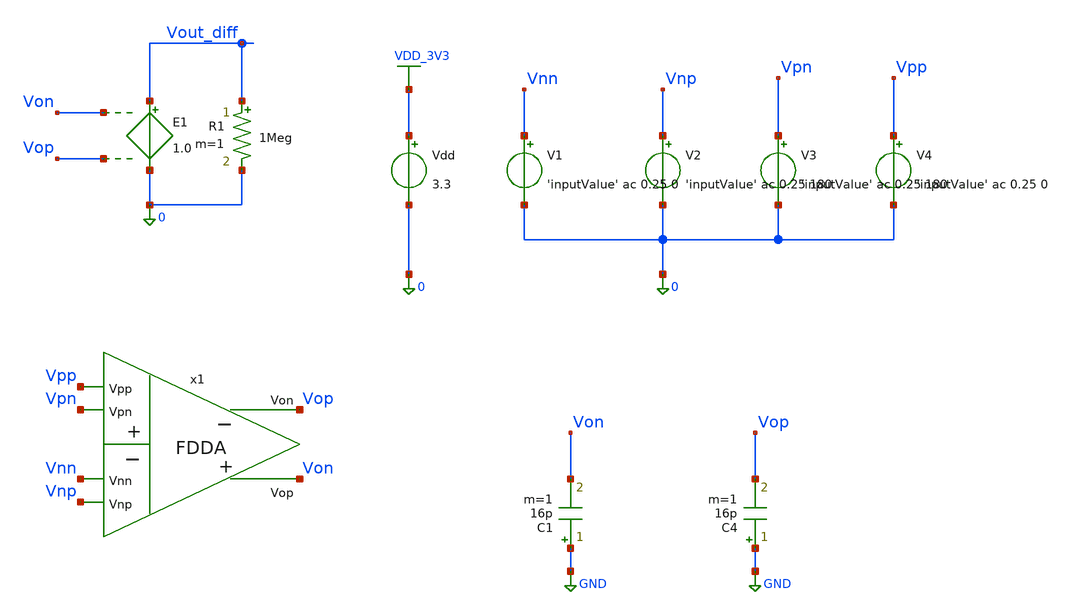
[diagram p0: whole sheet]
** sch_path: src/sim/sim_ac.sch
**.subckt sim_ac
V1 Vnn 0 'inputValue' ac 0.25 0
.save i(v1)
V2 Vnp 0 'inputValue' ac 0.25 180
.save i(v2)
V3 Vpn 0 'inputValue' ac 0.25 180
.save i(v3)
V4 Vpp 0 'inputValue' ac 0.25 0
.save i(v4)
Vdd VDD_3V3 0 3.3
.save i(vdd)
C1 GND Von 16p m=1
C4 GND Vop 16p m=1
x1 Vop Von Vnp Vnn Vpp Vpn fdda_subckt
E1 Vout_diff 0 Von Vop 1.0
R1 Vout_diff 0 1Meg m=1
**** begin user architecture code

.include $::180MCU_MODELS/design.ngspice
.lib $::180MCU_MODELS/sm141064.ngspice typical
.lib $::180MCU_MODELS/sm141064.ngspice cap_mim
.lib $::180MCU_MODELS/sm141064.ngspice res_typical
.lib $::180MCU_MODELS/sm141064.ngspice moscap_typical
.lib $::180MCU_MODELS/sm141064.ngspice mimcap_typical




.param inputValue=1.65
.global VDD_3V3

.control
  save all
  ac dec 1000 1 100Meg

  let Vop_db = db(Vop)
  let Vop_ph = phase(Vop)*180/pi
  let Von_db = db(Von)
  let Von_ph = phase(Von)*180/pi
  let Vout_diff_db = db(Vout_diff)
  let Vout_diff_ph = phase(Vout_diff)*180/pi

  write sim_ac.raw
.endc


**** end user architecture code
**.ends
.GLOBAL VDD_3V3
.GLOBAL GND
.end
